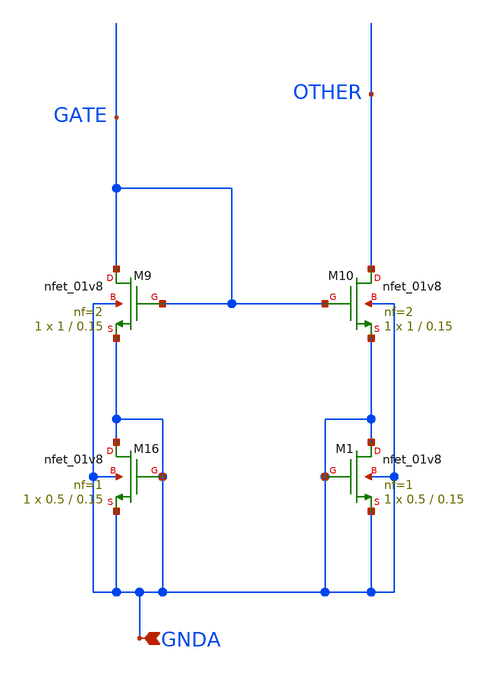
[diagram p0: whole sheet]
** sch_path: projects/pll/charge_pump/magic/example_xschem.sch
**.subckt example_xschem GNDA
*.ipin GNDA
XM9 GATE GATE GNDA GNDA sky130_fd_pr__nfet_01v8 L=0.15 W=1 nf=2 ad='int((nf+1)/2) * W/nf * 0.29' as='int((nf+2)/2) * W/nf * 0.29'
+ pd='2*int((nf+1)/2) * (W/nf + 0.29)' ps='2*int((nf+2)/2) * (W/nf + 0.29)' nrd='0.29 / W' nrs='0.29 / W'
+ sa=0 sb=0 sd=0 mult=1 m=1
XM10 OTHER GATE GNDA GNDA sky130_fd_pr__nfet_01v8 L=0.15 W=1 nf=2 ad='int((nf+1)/2) * W/nf * 0.29' as='int((nf+2)/2) * W/nf * 0.29'
+ pd='2*int((nf+1)/2) * (W/nf + 0.29)' ps='2*int((nf+2)/2) * (W/nf + 0.29)' nrd='0.29 / W' nrs='0.29 / W'
+ sa=0 sb=0 sd=0 mult=1 m=1
XM16 GNDA GNDA GNDA GNDA sky130_fd_pr__nfet_01v8 L=0.15 W=0.5 nf=1 ad='int((nf+1)/2) * W/nf * 0.29' as='int((nf+2)/2) * W/nf * 0.29'
+ pd='2*int((nf+1)/2) * (W/nf + 0.29)' ps='2*int((nf+2)/2) * (W/nf + 0.29)' nrd='0.29 / W' nrs='0.29 / W'
+ sa=0 sb=0 sd=0 mult=1 m=1
XM1 GNDA GNDA GNDA GNDA sky130_fd_pr__nfet_01v8 L=0.15 W=0.5 nf=1 ad='int((nf+1)/2) * W/nf * 0.29' as='int((nf+2)/2) * W/nf * 0.29'
+ pd='2*int((nf+1)/2) * (W/nf + 0.29)' ps='2*int((nf+2)/2) * (W/nf + 0.29)' nrd='0.29 / W' nrs='0.29 / W'
+ sa=0 sb=0 sd=0 mult=1 m=1
**.ends
.end
